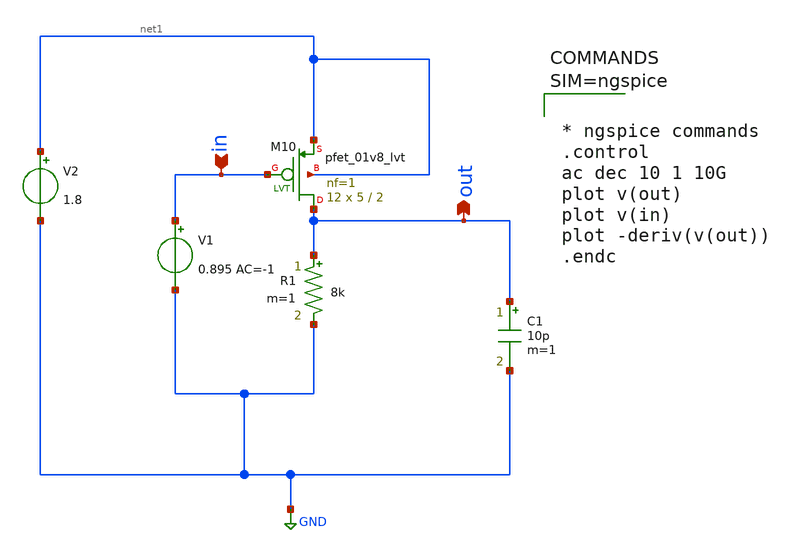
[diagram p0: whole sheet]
** sch_path: xschem/pmos_ac.sch
**.subckt pmos_ac in out
*.ipin in
*.opin out
XM10 out in net1 net1 sky130_fd_pr__pfet_01v8_lvt L=2 W=5 nf=1 ad='int((1 + 1)/2) * 5 / 1 * 0.29' as='int((1 + 2)/2) * 5 / 1 * 0.29'
+ pd='2*int((1 + 1)/2) * (5 / 1 + 0.29)' ps='2*int((1 + 2)/2) * (5 / 1 + 0.29)' nrd='0.29 / 5 ' nrs='0.29 / 5 '
+ sa=0 sb=0 sd=0 mult=12 m=12
R1 out GND 8k m=1
V1 in GND 0.895 AC=-1
C1 out GND 10p m=1
V2 net1 GND 1.8
**** begin user architecture code

** opencircuitdesign pdks install
.lib $::SKYWATER_MODELS/sky130.lib.spice tt




* ngspice commands
.control
ac dec 10 1 10G
plot v(out)
plot v(in)
plot -deriv(v(out))
.endc



**** end user architecture code
**.ends
.GLOBAL GND
.end
